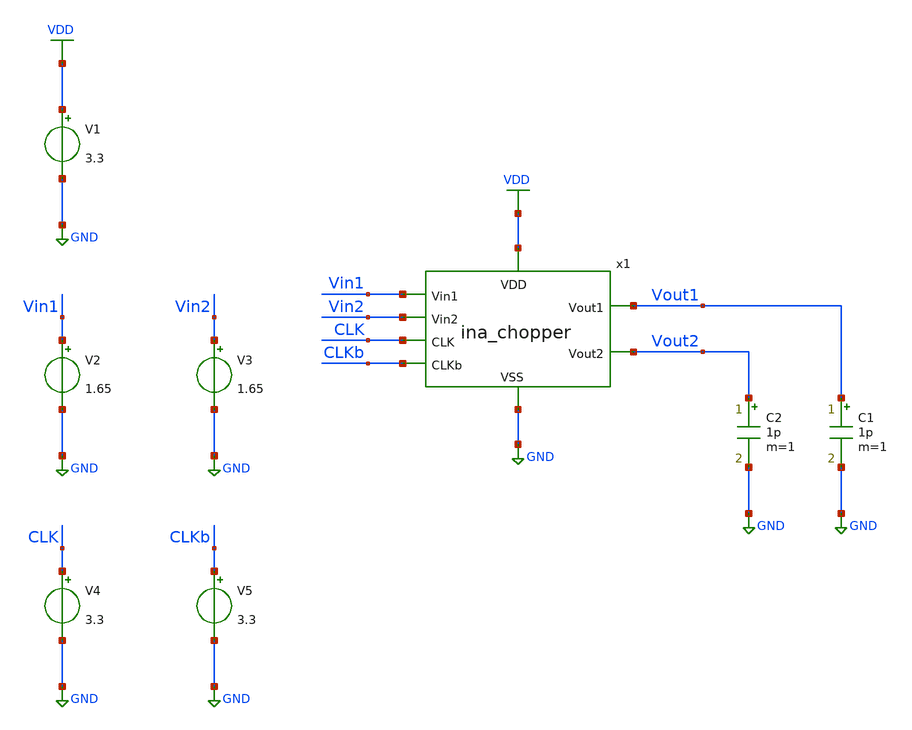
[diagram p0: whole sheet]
** sch_path: designs/libs/tb_ina/tb_ina_chopper_op/tb_ina_chopper_op.sch
**.subckt tb_ina_chopper_op
V1 VDD GND 3.3
V2 Vin1 GND 1.65
V4 CLK GND 3.3
V5 CLKb GND 3.3
V3 Vin2 GND 1.65
C2 Vout2 GND 1p m=1
C1 Vout1 GND 1p m=1
x1 Vout2 Vin1 VDD GND CLKb CLK Vout1 Vin2 ina_chopper
**** begin user architecture code

.include $::180MCU_MODELS/design.ngspice
.lib $::180MCU_MODELS/sm141064.ngspice typical
.lib $::180MCU_MODELS/sm141064.ngspice cap_mim
.lib $::180MCU_MODELS/sm141064.ngspice moscap_typical
.lib $::180MCU_MODELS/sm141064.ngspice mimcap_typical
.lib $::180MCU_MODELS/sm141064.ngspice res_typical
* .lib $::180MCU_MODELS/sm141064.ngspice res_statistical
* ngspice commands




.control
save all

set color0 = white

*************************************
** PARAMETERS
*************************************

let Vdd  = 3.3
let Vcm  = 1.65

*************************************
** SOURCES
*************************************

alter @V1[DC] = $&Vdd
alter @V2[DC] = $&Vcm
alter @V3[DC] = $&Vcm

*************************************
** TRANSMISSION GATE ON
*************************************

alter @V4[DC] = $&Vdd
alter @V5[DC] = 0

*************************************
** OPERATING POINT SIMULATION
*************************************

op

*************************************
** PRINT RESULTS
*************************************

echo ------ TG ON --------
echo ------ NMOS ---------
let XM1_vgs = @m.x1.xm1.m0[vgs]
let XM1_vds = @m.x1.xm1.m0[vds]
let XM1_id = @m.x1.xm1.m0[id]
let XM1_gm = @m.x1.xm1.m0[gm]
let XM1_gds = @m.x1.xm1.m0[gds]
let XM1_cgg = @m.x1.xm1.m0[cgg]
let XM1_ron = 1/@m.x1.xm1.m0[gds]
print XM1_vgs
print XM1_vds
print XM1_id
print XM1_gm
print XM1_gds
print XM1_cgg
print XM1_ron
echo ------ PMOS ---------
let XM2_vgs = @m.x1.xm2.m0[vgs]
let XM2_vds = @m.x1.xm2.m0[vds]
let XM2_id = @m.x1.xm2.m0[id]
let XM2_gm = @m.x1.xm2.m0[gm]
let XM2_gds = @m.x1.xm2.m0[gds]
let XM2_cgg = @m.x1.xm2.m0[cgg]
let XM2_ron = 1/@m.x1.xm2.m0[gds]
print XM2_vgs
print XM2_vds
print XM2_id
print XM2_gm
print XM2_gds
print XM2_cgg
print XM2_ron
echo ------ TG -----------
let Ron1 = 1/(XM1_gds + XM2_gds)
let Roff2 = 1/(@m.x1.xm3.m0[gds] + @m.x1.xm4.m0[gds])
let Ron3 = 1/(@m.x1.xm5.m0[gds] + @m.x1.xm6.m0[gds])
let Roff4 = 1/(@m.x1.xm7.m0[gds] + @m.x1.xm8.m0[gds])
let Ileak2 = abs(@m.x1.xm3.m0[id]) + abs(@m.x1.xm4.m0[id])
let Ileak4 = abs(@m.x1.xm7.m0[id]) + abs(@m.x1.xm8.m0[id])
let Ileak_tot = Ileak2 + Ileak4
print Ron1
print Roff2
print Ron3
print Roff4
print Ileak2
print Ileak4
print Ileak_tot

*************************************
** SAVE
*************************************

write tb_ina_chopper_op1.raw

*************************************
** TRANSMISSION GATE OFF
*************************************

alter @V4[DC] = 0
alter @V5[DC] = $&Vdd

*************************************
** OPERATING POINT SIMULATION
*************************************

op

*************************************
** PRINT RESULTS
*************************************

echo ------ TG OFF -------
echo ------ NMOS ---------
let XM1_vgs = @m.x1.xm1.m0[vgs]
let XM1_vds = @m.x1.xm1.m0[vds]
let XM1_id = @m.x1.xm1.m0[id]
let XM1_gm = @m.x1.xm1.m0[gm]
let XM1_gds = @m.x1.xm1.m0[gds]
let XM1_cgg = @m.x1.xm1.m0[cgg]
let XM1_roff = 1/@m.x1.xm1.m0[gds]
print XM1_vgs
print XM1_vds
print XM1_id
print XM1_gm
print XM1_gds
print XM1_cgg
print XM1_roff
echo ------ PMOS ---------
let XM2_vgs = @m.x1.xm2.m0[vgs]
let XM2_vds = @m.x1.xm2.m0[vds]
let XM2_id = @m.x1.xm2.m0[id]
let XM2_gm = @m.x1.xm2.m0[gm]
let XM2_gds = @m.x1.xm2.m0[gds]
let XM2_cgg = @m.x1.xm2.m0[cgg]
let XM2_roff = 1/@m.x1.xm2.m0[gds]
print XM2_vgs
print XM2_vds
print XM2_id
print XM2_gm
print XM2_gds
print XM2_cgg
print XM2_roff
echo ------ TG -----------
let Roff1 = 1/(XM1_gds + XM2_gds)
let Ron2 = 1/(@m.x1.xm3.m0[gds] + @m.x1.xm4.m0[gds])
let Roff3 = 1/(@m.x1.xm5.m0[gds] + @m.x1.xm6.m0[gds])
let Ron4 = 1/(@m.x1.xm7.m0[gds] + @m.x1.xm8.m0[gds])
let Ileak1 = abs(@m.x1.xm1.m0[id]) + abs(@m.x1.xm2.m0[id])
let Ileak3 = abs(@m.x1.xm5.m0[id]) + abs(@m.x1.xm6.m0[id])
let Ileak_tot = Ileak1 + Ileak3
print Roff1
print Ron2
print Roff3
print Ron4
print Ileak1
print Ileak3
print Ileak_tot

*************************************
** SAVE
*************************************

write tb_ina_chopper_op2.raw

.endc
* ngspice commands



**** end user architecture code
**.ends

* expanding   symbol:  libs/core_ina/ina_chopper/ina_chopper.sym # of pins=8
** sym_path: designs/libs/core_ina/ina_chopper/ina_chopper.sym
** sch_path: designs/libs/core_ina/ina_chopper/ina_chopper.sch
.subckt ina_chopper Vout2 Vin1 VDD VSS CLKb CLK Vout1 Vin2
*.ipin Vin1
*.ipin Vin2
*.ipin CLKb
*.opin Vout2
*.ipin CLK
*.opin Vout1
*.ipin VDD
*.ipin VSS
XM1 Vout1 CLK Vin1 VSS nfet_03v3 L=0.28u W=5u nf=1 ad='int((nf+1)/2) * W/nf * 0.18u' as='int((nf+2)/2) * W/nf * 0.18u'
+ pd='2*int((nf+1)/2) * (W/nf + 0.18u)' ps='2*int((nf+2)/2) * (W/nf + 0.18u)' nrd='0.18u / W' nrs='0.18u / W'
+ sa=0 sb=0 sd=0 m=1
XM2 Vout1 CLKb Vin1 VDD pfet_03v3 L=0.28u W=10u nf=1 ad='int((nf+1)/2) * W/nf * 0.18u' as='int((nf+2)/2) * W/nf * 0.18u'
+ pd='2*int((nf+1)/2) * (W/nf + 0.18u)' ps='2*int((nf+2)/2) * (W/nf + 0.18u)' nrd='0.18u / W' nrs='0.18u / W'
+ sa=0 sb=0 sd=0 m=1
XM3 Vout2 CLKb Vin1 VSS nfet_03v3 L=0.28u W=5u nf=1 ad='int((nf+1)/2) * W/nf * 0.18u' as='int((nf+2)/2) * W/nf * 0.18u'
+ pd='2*int((nf+1)/2) * (W/nf + 0.18u)' ps='2*int((nf+2)/2) * (W/nf + 0.18u)' nrd='0.18u / W' nrs='0.18u / W'
+ sa=0 sb=0 sd=0 m=1
XM4 Vout2 CLK Vin1 VDD pfet_03v3 L=0.28u W=10u nf=1 ad='int((nf+1)/2) * W/nf * 0.18u' as='int((nf+2)/2) * W/nf * 0.18u'
+ pd='2*int((nf+1)/2) * (W/nf + 0.18u)' ps='2*int((nf+2)/2) * (W/nf + 0.18u)' nrd='0.18u / W' nrs='0.18u / W'
+ sa=0 sb=0 sd=0 m=1
XM5 Vin2 CLK Vout2 VSS nfet_03v3 L=0.28u W=5u nf=1 ad='int((nf+1)/2) * W/nf * 0.18u' as='int((nf+2)/2) * W/nf * 0.18u'
+ pd='2*int((nf+1)/2) * (W/nf + 0.18u)' ps='2*int((nf+2)/2) * (W/nf + 0.18u)' nrd='0.18u / W' nrs='0.18u / W'
+ sa=0 sb=0 sd=0 m=1
XM6 Vin2 CLKb Vout2 VDD pfet_03v3 L=0.28u W=10u nf=1 ad='int((nf+1)/2) * W/nf * 0.18u' as='int((nf+2)/2) * W/nf * 0.18u'
+ pd='2*int((nf+1)/2) * (W/nf + 0.18u)' ps='2*int((nf+2)/2) * (W/nf + 0.18u)' nrd='0.18u / W' nrs='0.18u / W'
+ sa=0 sb=0 sd=0 m=1
XM7 Vin2 CLKb Vout1 VSS nfet_03v3 L=0.28u W=5u nf=1 ad='int((nf+1)/2) * W/nf * 0.18u' as='int((nf+2)/2) * W/nf * 0.18u'
+ pd='2*int((nf+1)/2) * (W/nf + 0.18u)' ps='2*int((nf+2)/2) * (W/nf + 0.18u)' nrd='0.18u / W' nrs='0.18u / W'
+ sa=0 sb=0 sd=0 m=1
XM8 Vin2 CLK Vout1 VDD pfet_03v3 L=0.28u W=10u nf=1 ad='int((nf+1)/2) * W/nf * 0.18u' as='int((nf+2)/2) * W/nf * 0.18u'
+ pd='2*int((nf+1)/2) * (W/nf + 0.18u)' ps='2*int((nf+2)/2) * (W/nf + 0.18u)' nrd='0.18u / W' nrs='0.18u / W'
+ sa=0 sb=0 sd=0 m=1
.ends

.GLOBAL GND
.GLOBAL VDD
.end
